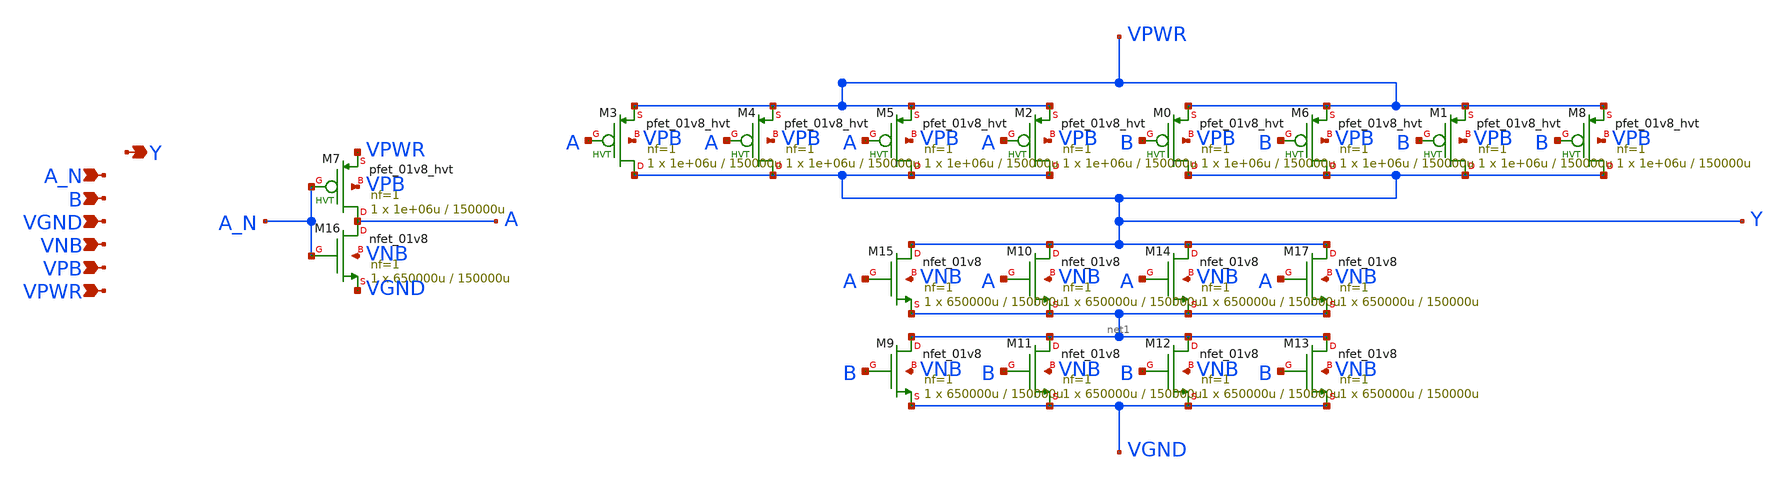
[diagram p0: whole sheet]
** sch_path: schematics/nand2b/sky130_fd_sc_hd__nand2b_4.sch
**.subckt sky130_fd_sc_hd__nand2b_4 A_N B VGND VNB VPB VPWR Y
*.ipin A_N
*.ipin B
*.ipin VGND
*.ipin VNB
*.ipin VPB
*.ipin VPWR
*.opin Y
XM0 Y B VPWR VPB sky130_fd_pr__pfet_01v8_hvt L=150000u W=1e+06u nf=1 ad='int((1 + 1)/2) * 1e+06u / 1 * 0.29'
+ as='int((1 + 2)/2) * 1e+06u / 1 * 0.29' pd='2*int((1 + 1)/2) * (1e+06u / 1 + 0.29)' ps='2*int((1 + 2)/2) * (1e+06u / 1 + 0.29)'
+ nrd='0.29 / 1e+06u ' nrs='0.29 / 1e+06u ' sa=0 sb=0 sd=0 mult=1 m=1
XM1 Y B VPWR VPB sky130_fd_pr__pfet_01v8_hvt L=150000u W=1e+06u nf=1 ad='int((1 + 1)/2) * 1e+06u / 1 * 0.29'
+ as='int((1 + 2)/2) * 1e+06u / 1 * 0.29' pd='2*int((1 + 1)/2) * (1e+06u / 1 + 0.29)' ps='2*int((1 + 2)/2) * (1e+06u / 1 + 0.29)'
+ nrd='0.29 / 1e+06u ' nrs='0.29 / 1e+06u ' sa=0 sb=0 sd=0 mult=1 m=1
XM2 Y A VPWR VPB sky130_fd_pr__pfet_01v8_hvt L=150000u W=1e+06u nf=1 ad='int((1 + 1)/2) * 1e+06u / 1 * 0.29'
+ as='int((1 + 2)/2) * 1e+06u / 1 * 0.29' pd='2*int((1 + 1)/2) * (1e+06u / 1 + 0.29)' ps='2*int((1 + 2)/2) * (1e+06u / 1 + 0.29)'
+ nrd='0.29 / 1e+06u ' nrs='0.29 / 1e+06u ' sa=0 sb=0 sd=0 mult=1 m=1
XM3 Y A VPWR VPB sky130_fd_pr__pfet_01v8_hvt L=150000u W=1e+06u nf=1 ad='int((1 + 1)/2) * 1e+06u / 1 * 0.29'
+ as='int((1 + 2)/2) * 1e+06u / 1 * 0.29' pd='2*int((1 + 1)/2) * (1e+06u / 1 + 0.29)' ps='2*int((1 + 2)/2) * (1e+06u / 1 + 0.29)'
+ nrd='0.29 / 1e+06u ' nrs='0.29 / 1e+06u ' sa=0 sb=0 sd=0 mult=1 m=1
XM4 Y A VPWR VPB sky130_fd_pr__pfet_01v8_hvt L=150000u W=1e+06u nf=1 ad='int((1 + 1)/2) * 1e+06u / 1 * 0.29'
+ as='int((1 + 2)/2) * 1e+06u / 1 * 0.29' pd='2*int((1 + 1)/2) * (1e+06u / 1 + 0.29)' ps='2*int((1 + 2)/2) * (1e+06u / 1 + 0.29)'
+ nrd='0.29 / 1e+06u ' nrs='0.29 / 1e+06u ' sa=0 sb=0 sd=0 mult=1 m=1
XM5 Y A VPWR VPB sky130_fd_pr__pfet_01v8_hvt L=150000u W=1e+06u nf=1 ad='int((1 + 1)/2) * 1e+06u / 1 * 0.29'
+ as='int((1 + 2)/2) * 1e+06u / 1 * 0.29' pd='2*int((1 + 1)/2) * (1e+06u / 1 + 0.29)' ps='2*int((1 + 2)/2) * (1e+06u / 1 + 0.29)'
+ nrd='0.29 / 1e+06u ' nrs='0.29 / 1e+06u ' sa=0 sb=0 sd=0 mult=1 m=1
XM6 Y B VPWR VPB sky130_fd_pr__pfet_01v8_hvt L=150000u W=1e+06u nf=1 ad='int((1 + 1)/2) * 1e+06u / 1 * 0.29'
+ as='int((1 + 2)/2) * 1e+06u / 1 * 0.29' pd='2*int((1 + 1)/2) * (1e+06u / 1 + 0.29)' ps='2*int((1 + 2)/2) * (1e+06u / 1 + 0.29)'
+ nrd='0.29 / 1e+06u ' nrs='0.29 / 1e+06u ' sa=0 sb=0 sd=0 mult=1 m=1
XM7 A A_N VPWR VPB sky130_fd_pr__pfet_01v8_hvt L=150000u W=1e+06u nf=1 ad='int((1 + 1)/2) * 1e+06u / 1 * 0.29'
+ as='int((1 + 2)/2) * 1e+06u / 1 * 0.29' pd='2*int((1 + 1)/2) * (1e+06u / 1 + 0.29)' ps='2*int((1 + 2)/2) * (1e+06u / 1 + 0.29)'
+ nrd='0.29 / 1e+06u ' nrs='0.29 / 1e+06u ' sa=0 sb=0 sd=0 mult=1 m=1
XM8 Y B VPWR VPB sky130_fd_pr__pfet_01v8_hvt L=150000u W=1e+06u nf=1 ad='int((1 + 1)/2) * 1e+06u / 1 * 0.29'
+ as='int((1 + 2)/2) * 1e+06u / 1 * 0.29' pd='2*int((1 + 1)/2) * (1e+06u / 1 + 0.29)' ps='2*int((1 + 2)/2) * (1e+06u / 1 + 0.29)'
+ nrd='0.29 / 1e+06u ' nrs='0.29 / 1e+06u ' sa=0 sb=0 sd=0 mult=1 m=1
XM9 net1 B VGND VNB sky130_fd_pr__nfet_01v8 L=150000u W=650000u nf=1 ad='int((1 + 1)/2) * 650000u / 1 * 0.29'
+ as='int((1 + 2)/2) * 650000u / 1 * 0.29' pd='2*int((1 + 1)/2) * (650000u / 1 + 0.29)' ps='2*int((1 + 2)/2) * (650000u / 1 + 0.29)'
+ nrd='0.29 / 650000u ' nrs='0.29 / 650000u ' sa=0 sb=0 sd=0 mult=1 m=1
XM10 Y A net1 VNB sky130_fd_pr__nfet_01v8 L=150000u W=650000u nf=1 ad='int((1 + 1)/2) * 650000u / 1 * 0.29'
+ as='int((1 + 2)/2) * 650000u / 1 * 0.29' pd='2*int((1 + 1)/2) * (650000u / 1 + 0.29)' ps='2*int((1 + 2)/2) * (650000u / 1 + 0.29)'
+ nrd='0.29 / 650000u ' nrs='0.29 / 650000u ' sa=0 sb=0 sd=0 mult=1 m=1
XM11 net1 B VGND VNB sky130_fd_pr__nfet_01v8 L=150000u W=650000u nf=1 ad='int((1 + 1)/2) * 650000u / 1 * 0.29'
+ as='int((1 + 2)/2) * 650000u / 1 * 0.29' pd='2*int((1 + 1)/2) * (650000u / 1 + 0.29)' ps='2*int((1 + 2)/2) * (650000u / 1 + 0.29)'
+ nrd='0.29 / 650000u ' nrs='0.29 / 650000u ' sa=0 sb=0 sd=0 mult=1 m=1
XM12 net1 B VGND VNB sky130_fd_pr__nfet_01v8 L=150000u W=650000u nf=1 ad='int((1 + 1)/2) * 650000u / 1 * 0.29'
+ as='int((1 + 2)/2) * 650000u / 1 * 0.29' pd='2*int((1 + 1)/2) * (650000u / 1 + 0.29)' ps='2*int((1 + 2)/2) * (650000u / 1 + 0.29)'
+ nrd='0.29 / 650000u ' nrs='0.29 / 650000u ' sa=0 sb=0 sd=0 mult=1 m=1
XM13 net1 B VGND VNB sky130_fd_pr__nfet_01v8 L=150000u W=650000u nf=1 ad='int((1 + 1)/2) * 650000u / 1 * 0.29'
+ as='int((1 + 2)/2) * 650000u / 1 * 0.29' pd='2*int((1 + 1)/2) * (650000u / 1 + 0.29)' ps='2*int((1 + 2)/2) * (650000u / 1 + 0.29)'
+ nrd='0.29 / 650000u ' nrs='0.29 / 650000u ' sa=0 sb=0 sd=0 mult=1 m=1
XM14 Y A net1 VNB sky130_fd_pr__nfet_01v8 L=150000u W=650000u nf=1 ad='int((1 + 1)/2) * 650000u / 1 * 0.29'
+ as='int((1 + 2)/2) * 650000u / 1 * 0.29' pd='2*int((1 + 1)/2) * (650000u / 1 + 0.29)' ps='2*int((1 + 2)/2) * (650000u / 1 + 0.29)'
+ nrd='0.29 / 650000u ' nrs='0.29 / 650000u ' sa=0 sb=0 sd=0 mult=1 m=1
XM15 Y A net1 VNB sky130_fd_pr__nfet_01v8 L=150000u W=650000u nf=1 ad='int((1 + 1)/2) * 650000u / 1 * 0.29'
+ as='int((1 + 2)/2) * 650000u / 1 * 0.29' pd='2*int((1 + 1)/2) * (650000u / 1 + 0.29)' ps='2*int((1 + 2)/2) * (650000u / 1 + 0.29)'
+ nrd='0.29 / 650000u ' nrs='0.29 / 650000u ' sa=0 sb=0 sd=0 mult=1 m=1
XM16 A A_N VGND VNB sky130_fd_pr__nfet_01v8 L=150000u W=650000u nf=1 ad='int((1 + 1)/2) * 650000u / 1 * 0.29'
+ as='int((1 + 2)/2) * 650000u / 1 * 0.29' pd='2*int((1 + 1)/2) * (650000u / 1 + 0.29)' ps='2*int((1 + 2)/2) * (650000u / 1 + 0.29)'
+ nrd='0.29 / 650000u ' nrs='0.29 / 650000u ' sa=0 sb=0 sd=0 mult=1 m=1
XM17 Y A net1 VNB sky130_fd_pr__nfet_01v8 L=150000u W=650000u nf=1 ad='int((1 + 1)/2) * 650000u / 1 * 0.29'
+ as='int((1 + 2)/2) * 650000u / 1 * 0.29' pd='2*int((1 + 1)/2) * (650000u / 1 + 0.29)' ps='2*int((1 + 2)/2) * (650000u / 1 + 0.29)'
+ nrd='0.29 / 650000u ' nrs='0.29 / 650000u ' sa=0 sb=0 sd=0 mult=1 m=1
**.ends
.end
